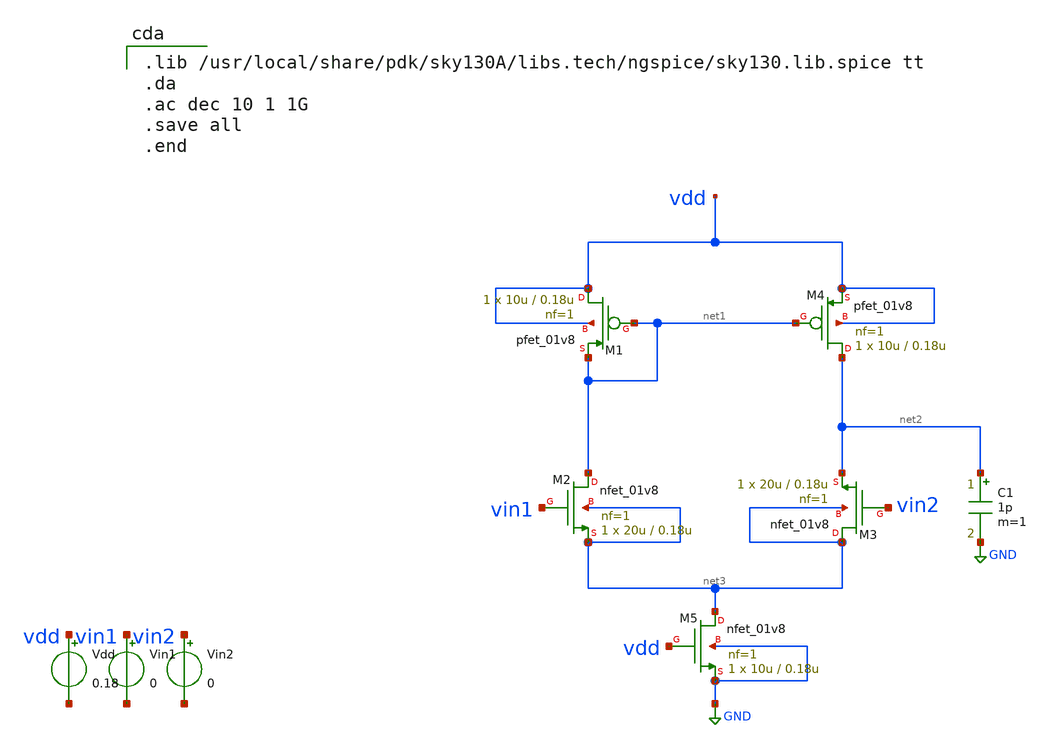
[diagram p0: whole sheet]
** sch_path: differentialamlifier.sch
**.subckt differentialamlifier
XM1 vdd net1 net1 vdd sky130_fd_pr__pfet_01v8 L=0.18u W=10u nf=1 ad='int((1 + 1)/2) * 10u / 1 * 0.29'
+ as='int((1 + 2)/2) * 10u / 1 * 0.29' pd='2*int((1 + 1)/2) * (10u / 1 + 0.29)' ps='2*int((1 + 2)/2) * (10u / 1 + 0.29)'
+ nrd='0.29 / 10u ' nrs='0.29 / 10u ' sa=0 sb=0 sd=0 mult=1 m=1
XM2 net1 vin1 net3 net3 sky130_fd_pr__nfet_01v8 L=0.18u W=20u nf=1 ad='int((1 + 1)/2) * 20u / 1 * 0.29'
+ as='int((1 + 2)/2) * 20u / 1 * 0.29' pd='2*int((1 + 1)/2) * (20u / 1 + 0.29)' ps='2*int((1 + 2)/2) * (20u / 1 + 0.29)'
+ nrd='0.29 / 20u ' nrs='0.29 / 20u ' sa=0 sb=0 sd=0 mult=1 m=1
C1 net2 GND 1p m=1
Vdd vdd net4 0.18
XM3 net3 vin2 net2 net3 sky130_fd_pr__nfet_01v8 L=0.18u W=20u nf=1 ad='int((1 + 1)/2) * 20u / 1 * 0.29'
+ as='int((1 + 2)/2) * 20u / 1 * 0.29' pd='2*int((1 + 1)/2) * (20u / 1 + 0.29)' ps='2*int((1 + 2)/2) * (20u / 1 + 0.29)'
+ nrd='0.29 / 20u ' nrs='0.29 / 20u ' sa=0 sb=0 sd=0 mult=1 m=1
XM4 net2 net1 vdd vdd sky130_fd_pr__pfet_01v8 L=0.18u W=10u nf=1 ad='int((1 + 1)/2) * 10u / 1 * 0.29'
+ as='int((1 + 2)/2) * 10u / 1 * 0.29' pd='2*int((1 + 1)/2) * (10u / 1 + 0.29)' ps='2*int((1 + 2)/2) * (10u / 1 + 0.29)'
+ nrd='0.29 / 10u ' nrs='0.29 / 10u ' sa=0 sb=0 sd=0 mult=1 m=1
XM5 net3 vdd GND GND sky130_fd_pr__nfet_01v8 L=0.18u W=10u nf=1 ad='int((1 + 1)/2) * 10u / 1 * 0.29'
+ as='int((1 + 2)/2) * 10u / 1 * 0.29' pd='2*int((1 + 1)/2) * (10u / 1 + 0.29)' ps='2*int((1 + 2)/2) * (10u / 1 + 0.29)'
+ nrd='0.29 / 10u ' nrs='0.29 / 10u ' sa=0 sb=0 sd=0 mult=1 m=1
Vin1 vin1 net5 0
Vin2 vin2 net6 0
**** begin user architecture code

.lib /usr/local/share/pdk/sky130A/libs.tech/ngspice/sky130.lib.spice tt
.da
.ac dec 10 1 1G
.save all
.end

**** end user architecture code
**.ends
.GLOBAL GND
.end
